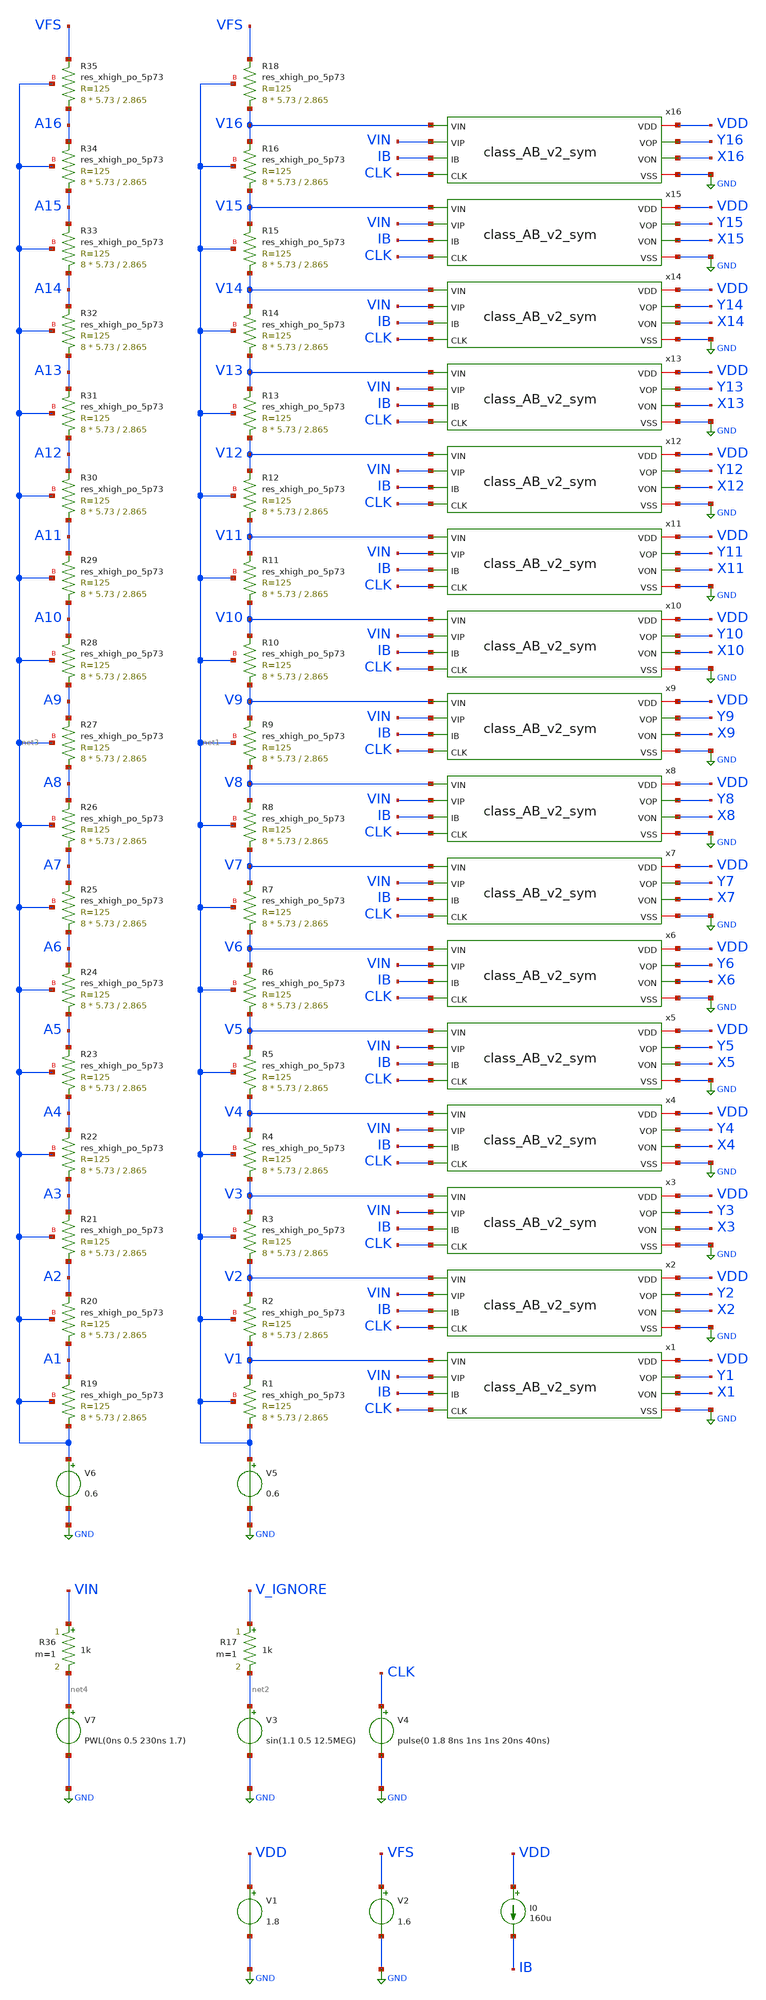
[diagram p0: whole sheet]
** sch_path: strongARM/flash_ADC_4b_v2.sch
**.subckt flash_ADC_4b_v2
V3 net2 GND sin(1.1 0.5 12.5MEG)
V4 CLK GND pulse(0 1.8 8ns 1ns 1ns 20ns 40ns)
V1 VDD GND 1.8
V2 VFS GND 1.6
R17 V_IGNORE net2 1k m=1
I0 VDD IB 160u
V5 net1 GND 0.6
XR19 net3 A1 net3 sky130_fd_pr__res_xhigh_po_5p73 L=2.865 mult=8 m=8
V6 net3 GND 0.6
XR20 A1 A2 net3 sky130_fd_pr__res_xhigh_po_5p73 L=2.865 mult=8 m=8
XR21 A2 A3 net3 sky130_fd_pr__res_xhigh_po_5p73 L=2.865 mult=8 m=8
XR22 A3 A4 net3 sky130_fd_pr__res_xhigh_po_5p73 L=2.865 mult=8 m=8
XR23 A4 A5 net3 sky130_fd_pr__res_xhigh_po_5p73 L=2.865 mult=8 m=8
XR24 A5 A6 net3 sky130_fd_pr__res_xhigh_po_5p73 L=2.865 mult=8 m=8
XR25 A6 A7 net3 sky130_fd_pr__res_xhigh_po_5p73 L=2.865 mult=8 m=8
XR26 A7 A8 net3 sky130_fd_pr__res_xhigh_po_5p73 L=2.865 mult=8 m=8
XR27 A8 A9 net3 sky130_fd_pr__res_xhigh_po_5p73 L=2.865 mult=8 m=8
XR28 A9 A10 net3 sky130_fd_pr__res_xhigh_po_5p73 L=2.865 mult=8 m=8
XR29 A10 A11 net3 sky130_fd_pr__res_xhigh_po_5p73 L=2.865 mult=8 m=8
XR30 A11 A12 net3 sky130_fd_pr__res_xhigh_po_5p73 L=2.865 mult=8 m=8
XR31 A12 A13 net3 sky130_fd_pr__res_xhigh_po_5p73 L=2.865 mult=8 m=8
XR32 A13 A14 net3 sky130_fd_pr__res_xhigh_po_5p73 L=2.865 mult=8 m=8
XR33 A14 A15 net3 sky130_fd_pr__res_xhigh_po_5p73 L=2.865 mult=8 m=8
XR34 A15 A16 net3 sky130_fd_pr__res_xhigh_po_5p73 L=2.865 mult=8 m=8
XR35 A16 VFS net3 sky130_fd_pr__res_xhigh_po_5p73 L=2.865 mult=8 m=8
XR1 net1 V1 net1 sky130_fd_pr__res_xhigh_po_5p73 L=2.865 mult=8 m=8
XR2 V1 V2 net1 sky130_fd_pr__res_xhigh_po_5p73 L=2.865 mult=8 m=8
XR3 V2 V3 net1 sky130_fd_pr__res_xhigh_po_5p73 L=2.865 mult=8 m=8
XR4 V3 V4 net1 sky130_fd_pr__res_xhigh_po_5p73 L=2.865 mult=8 m=8
XR5 V4 V5 net1 sky130_fd_pr__res_xhigh_po_5p73 L=2.865 mult=8 m=8
XR6 V5 V6 net1 sky130_fd_pr__res_xhigh_po_5p73 L=2.865 mult=8 m=8
XR7 V6 V7 net1 sky130_fd_pr__res_xhigh_po_5p73 L=2.865 mult=8 m=8
XR8 V7 V8 net1 sky130_fd_pr__res_xhigh_po_5p73 L=2.865 mult=8 m=8
XR9 V8 V9 net1 sky130_fd_pr__res_xhigh_po_5p73 L=2.865 mult=8 m=8
XR10 V9 V10 net1 sky130_fd_pr__res_xhigh_po_5p73 L=2.865 mult=8 m=8
XR11 V10 V11 net1 sky130_fd_pr__res_xhigh_po_5p73 L=2.865 mult=8 m=8
XR12 V11 V12 net1 sky130_fd_pr__res_xhigh_po_5p73 L=2.865 mult=8 m=8
XR13 V12 V13 net1 sky130_fd_pr__res_xhigh_po_5p73 L=2.865 mult=8 m=8
XR14 V13 V14 net1 sky130_fd_pr__res_xhigh_po_5p73 L=2.865 mult=8 m=8
XR15 V14 V15 net1 sky130_fd_pr__res_xhigh_po_5p73 L=2.865 mult=8 m=8
XR16 V15 V16 net1 sky130_fd_pr__res_xhigh_po_5p73 L=2.865 mult=8 m=8
XR18 V16 VFS net1 sky130_fd_pr__res_xhigh_po_5p73 L=2.865 mult=8 m=8
V7 net4 GND PWL(0ns 0.5 230ns 1.7)
R36 VIN net4 1k m=1
x1 VDD Y1 X1 V1 VIN IB CLK GND class_AB_v2_sym
x2 VDD Y2 X2 V2 VIN IB CLK GND class_AB_v2_sym
x3 VDD Y3 X3 V3 VIN IB CLK GND class_AB_v2_sym
x4 VDD Y4 X4 V4 VIN IB CLK GND class_AB_v2_sym
x5 VDD Y5 X5 V5 VIN IB CLK GND class_AB_v2_sym
x6 VDD Y6 X6 V6 VIN IB CLK GND class_AB_v2_sym
x7 VDD Y7 X7 V7 VIN IB CLK GND class_AB_v2_sym
x8 VDD Y8 X8 V8 VIN IB CLK GND class_AB_v2_sym
x9 VDD Y9 X9 V9 VIN IB CLK GND class_AB_v2_sym
x10 VDD Y10 X10 V10 VIN IB CLK GND class_AB_v2_sym
x11 VDD Y11 X11 V11 VIN IB CLK GND class_AB_v2_sym
x12 VDD Y12 X12 V12 VIN IB CLK GND class_AB_v2_sym
x13 VDD Y13 X13 V13 VIN IB CLK GND class_AB_v2_sym
x14 VDD Y14 X14 V14 VIN IB CLK GND class_AB_v2_sym
x15 VDD Y15 X15 V15 VIN IB CLK GND class_AB_v2_sym
x16 VDD Y16 X16 V16 VIN IB CLK GND class_AB_v2_sym
**** begin user architecture code
.lib $::SKYWATER_MODELS/sky130.lib.spice tt


.options savecurrents
.control

save all

tran 0.005n 240n
remzerovec
write flash_ADC_4b_v2.raw

.endc


**** end user architecture code
**.ends

* expanding   symbol:  /foss/designs/Analog_FA23_SP24/strongARM/class_AB_v2_sym.sym # of pins=8
** sym_path: flashADC/xschem/class_AB_v2_sym.sym
** sch_path: flashADC/xschem/class_AB_v2_sym.sch
.subckt class_AB_v2_sym VDD VOP VON VIN VIP IB CLK VSS
*.iopin VDD
*.ipin IB
*.iopin VSS
*.ipin VIP
*.ipin VIN
*.opin VON
*.opin VOP
*.ipin CLK
XM17 net3 VIP VIR VSS sky130_fd_pr__nfet_01v8_lvt L=0.6 W=4 nf=1 ad='int((nf+1)/2) * W/nf * 0.29' as='int((nf+2)/2) * W/nf * 0.29'
+ pd='2*int((nf+1)/2) * (W/nf + 0.29)' ps='2*int((nf+2)/2) * (W/nf + 0.29)' nrd='0.29 / W' nrs='0.29 / W'
+ sa=0 sb=0 sd=0 mult=1 m=1
XM12 IB IB VSS VSS sky130_fd_pr__nfet_01v8_lvt L=0.6 W=4 nf=1 ad='int((nf+1)/2) * W/nf * 0.29' as='int((nf+2)/2) * W/nf * 0.29'
+ pd='2*int((nf+1)/2) * (W/nf + 0.29)' ps='2*int((nf+2)/2) * (W/nf + 0.29)' nrd='0.29 / W' nrs='0.29 / W'
+ sa=0 sb=0 sd=0 mult=1 m=1
XM15 net2 VIN VIR VSS sky130_fd_pr__nfet_01v8_lvt L=0.6 W=4 nf=1 ad='int((nf+1)/2) * W/nf * 0.29' as='int((nf+2)/2) * W/nf * 0.29'
+ pd='2*int((nf+1)/2) * (W/nf + 0.29)' ps='2*int((nf+2)/2) * (W/nf + 0.29)' nrd='0.29 / W' nrs='0.29 / W'
+ sa=0 sb=0 sd=0 mult=1 m=1
XM13 VIR IB VSS VSS sky130_fd_pr__nfet_01v8_lvt L=0.6 W=4 nf=1 ad='int((nf+1)/2) * W/nf * 0.29' as='int((nf+2)/2) * W/nf * 0.29'
+ pd='2*int((nf+1)/2) * (W/nf + 0.29)' ps='2*int((nf+2)/2) * (W/nf + 0.29)' nrd='0.29 / W' nrs='0.29 / W'
+ sa=0 sb=0 sd=0 mult=2 m=2
XM6 VON VOP VDD VDD sky130_fd_pr__pfet_01v8_lvt L=0.35 W=4 nf=1 ad='int((nf+1)/2) * W/nf * 0.29' as='int((nf+2)/2) * W/nf * 0.29'
+ pd='2*int((nf+1)/2) * (W/nf + 0.29)' ps='2*int((nf+2)/2) * (W/nf + 0.29)' nrd='0.29 / W' nrs='0.29 / W'
+ sa=0 sb=0 sd=0 mult=1 m=1
XM7 VOP VON VDD VDD sky130_fd_pr__pfet_01v8_lvt L=0.35 W=4 nf=1 ad='int((nf+1)/2) * W/nf * 0.29' as='int((nf+2)/2) * W/nf * 0.29'
+ pd='2*int((nf+1)/2) * (W/nf + 0.29)' ps='2*int((nf+2)/2) * (W/nf + 0.29)' nrd='0.29 / W' nrs='0.29 / W'
+ sa=0 sb=0 sd=0 mult=1 m=1
XM10 VOP VON net1 VSS sky130_fd_pr__nfet_01v8_lvt L=0.15 W=1 nf=1 ad='int((nf+1)/2) * W/nf * 0.29' as='int((nf+2)/2) * W/nf * 0.29'
+ pd='2*int((nf+1)/2) * (W/nf + 0.29)' ps='2*int((nf+2)/2) * (W/nf + 0.29)' nrd='0.29 / W' nrs='0.29 / W'
+ sa=0 sb=0 sd=0 mult=1 m=1
XM11 VON VOP net1 VSS sky130_fd_pr__nfet_01v8_lvt L=0.15 W=1 nf=1 ad='int((nf+1)/2) * W/nf * 0.29' as='int((nf+2)/2) * W/nf * 0.29'
+ pd='2*int((nf+1)/2) * (W/nf + 0.29)' ps='2*int((nf+2)/2) * (W/nf + 0.29)' nrd='0.29 / W' nrs='0.29 / W'
+ sa=0 sb=0 sd=0 mult=1 m=1
XM1 net1 CLK VSS VSS sky130_fd_pr__nfet_01v8_lvt L=0.15 W=1 nf=1 ad='int((nf+1)/2) * W/nf * 0.29' as='int((nf+2)/2) * W/nf * 0.29'
+ pd='2*int((nf+1)/2) * (W/nf + 0.29)' ps='2*int((nf+2)/2) * (W/nf + 0.29)' nrd='0.29 / W' nrs='0.29 / W'
+ sa=0 sb=0 sd=0 mult=1 m=1
XM2 VOP CLK VON VDD sky130_fd_pr__pfet_01v8_lvt L=0.35 W=4 nf=1 ad='int((nf+1)/2) * W/nf * 0.29' as='int((nf+2)/2) * W/nf * 0.29'
+ pd='2*int((nf+1)/2) * (W/nf + 0.29)' ps='2*int((nf+2)/2) * (W/nf + 0.29)' nrd='0.29 / W' nrs='0.29 / W'
+ sa=0 sb=0 sd=0 mult=1 m=1
XM5 net2 VIP net2 net2 sky130_fd_pr__nfet_01v8_lvt L=0.15 W=2 nf=1 ad='int((nf+1)/2) * W/nf * 0.29' as='int((nf+2)/2) * W/nf * 0.29'
+ pd='2*int((nf+1)/2) * (W/nf + 0.29)' ps='2*int((nf+2)/2) * (W/nf + 0.29)' nrd='0.29 / W' nrs='0.29 / W'
+ sa=0 sb=0 sd=0 mult=1 m=1
XM8 net3 VIN net3 net3 sky130_fd_pr__nfet_01v8_lvt L=0.15 W=2 nf=1 ad='int((nf+1)/2) * W/nf * 0.29' as='int((nf+2)/2) * W/nf * 0.29'
+ pd='2*int((nf+1)/2) * (W/nf + 0.29)' ps='2*int((nf+2)/2) * (W/nf + 0.29)' nrd='0.29 / W' nrs='0.29 / W'
+ sa=0 sb=0 sd=0 mult=1 m=1
XM9 net2 CLK VOP VDD sky130_fd_pr__pfet_01v8_lvt L=0.35 W=4 nf=1 ad='int((nf+1)/2) * W/nf * 0.29' as='int((nf+2)/2) * W/nf * 0.29'
+ pd='2*int((nf+1)/2) * (W/nf + 0.29)' ps='2*int((nf+2)/2) * (W/nf + 0.29)' nrd='0.29 / W' nrs='0.29 / W'
+ sa=0 sb=0 sd=0 mult=1 m=1
XM14 net3 CLK VON VDD sky130_fd_pr__pfet_01v8_lvt L=0.35 W=4 nf=1 ad='int((nf+1)/2) * W/nf * 0.29' as='int((nf+2)/2) * W/nf * 0.29'
+ pd='2*int((nf+1)/2) * (W/nf + 0.29)' ps='2*int((nf+2)/2) * (W/nf + 0.29)' nrd='0.29 / W' nrs='0.29 / W'
+ sa=0 sb=0 sd=0 mult=1 m=1
XM3 VDD CLK net3 VSS sky130_fd_pr__nfet_01v8_lvt L=0.6 W=4 nf=1 ad='int((nf+1)/2) * W/nf * 0.29' as='int((nf+2)/2) * W/nf * 0.29'
+ pd='2*int((nf+1)/2) * (W/nf + 0.29)' ps='2*int((nf+2)/2) * (W/nf + 0.29)' nrd='0.29 / W' nrs='0.29 / W'
+ sa=0 sb=0 sd=0 mult=1 m=1
XM4 VDD CLK net2 VSS sky130_fd_pr__nfet_01v8_lvt L=0.6 W=4 nf=1 ad='int((nf+1)/2) * W/nf * 0.29' as='int((nf+2)/2) * W/nf * 0.29'
+ pd='2*int((nf+1)/2) * (W/nf + 0.29)' ps='2*int((nf+2)/2) * (W/nf + 0.29)' nrd='0.29 / W' nrs='0.29 / W'
+ sa=0 sb=0 sd=0 mult=1 m=1
.ends

.GLOBAL GND
.end
